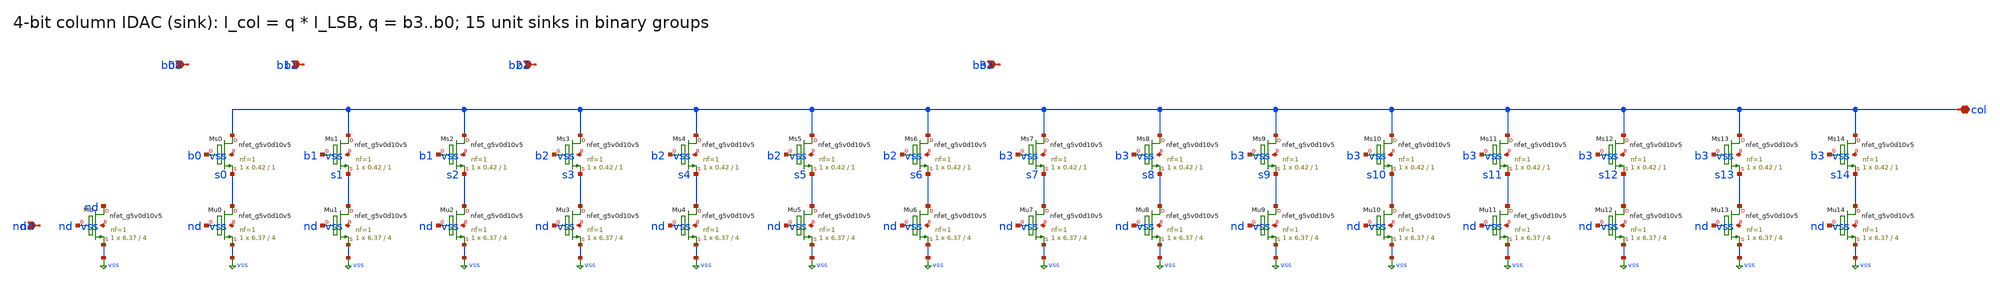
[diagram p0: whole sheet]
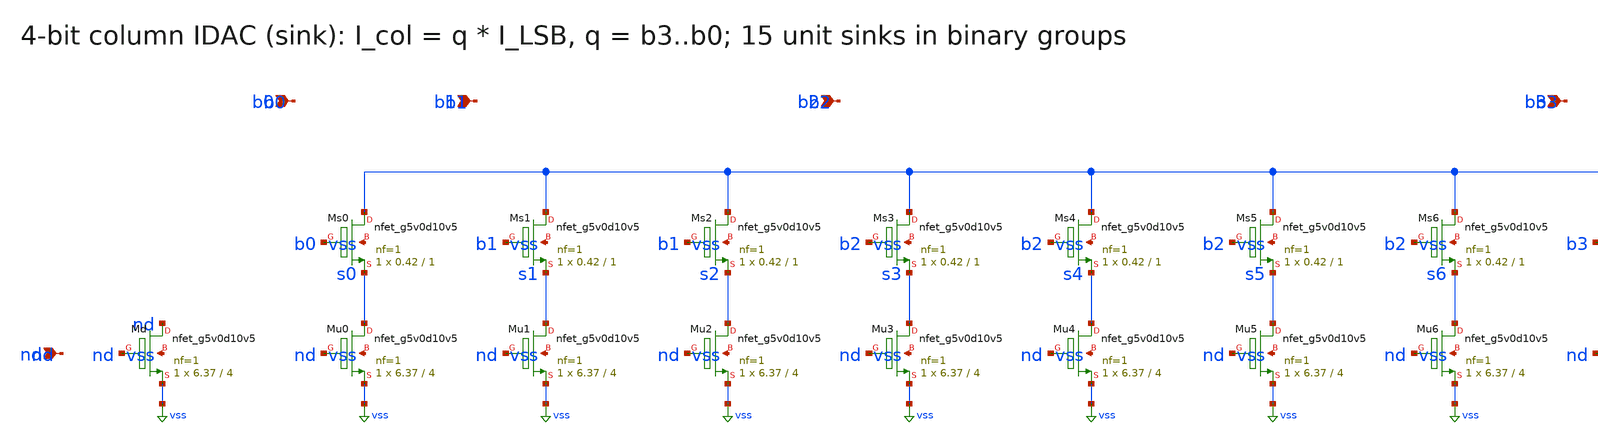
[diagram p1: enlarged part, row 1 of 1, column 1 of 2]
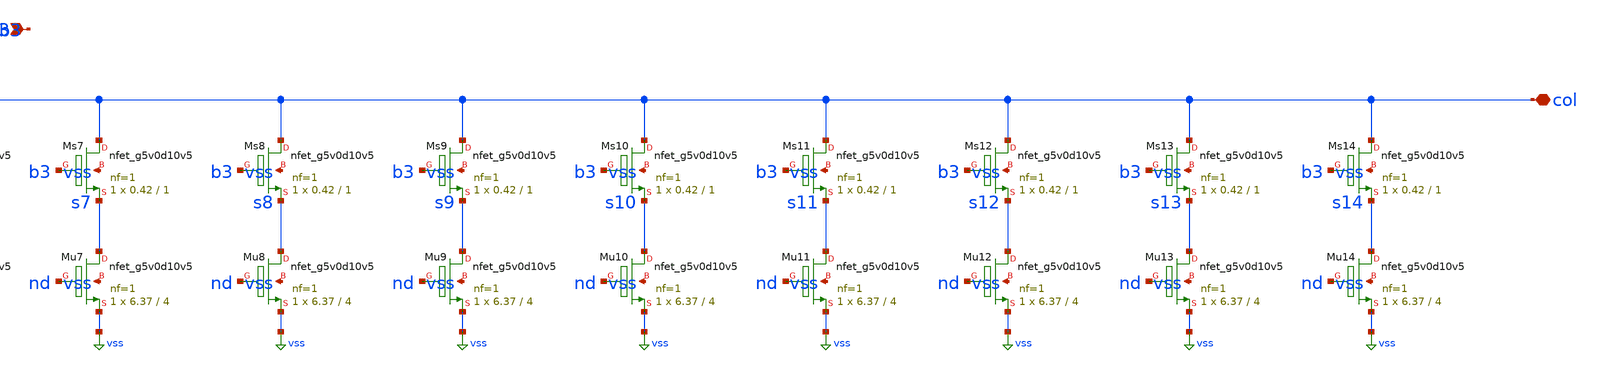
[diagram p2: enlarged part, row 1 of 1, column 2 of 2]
** sch_path: xschem/rt5w_idac4.sch
**.subckt rt5w_idac4 nd b0 b1 b2 b3 col
*.ipin nd
*.ipin b0
*.ipin b1
*.ipin b2
*.ipin b3
*.iopin col
XMd nd nd vss vss sky130_fd_pr__nfet_g5v0d10v5 L=4 W=6.37 nf=1 ad=1.847 as=1.847 pd=13.32 ps=13.32
+ nrd=0.04553 nrs=0.04553 sa=0 sb=0 sd=0 mult=1 m=1
XMu0 s0 nd vss vss sky130_fd_pr__nfet_g5v0d10v5 L=4 W=6.37 nf=1 ad=1.847 as=1.847 pd=13.32 ps=13.32
+ nrd=0.04553 nrs=0.04553 sa=0 sb=0 sd=0 mult=1 m=1
XMs0 col b0 s0 vss sky130_fd_pr__nfet_g5v0d10v5 L=1 W=0.42 nf=1 ad=0.1218 as=0.1218 pd=1.42 ps=1.42
+ nrd=0.6905 nrs=0.6905 sa=0 sb=0 sd=0 mult=1 m=1
XMu1 s1 nd vss vss sky130_fd_pr__nfet_g5v0d10v5 L=4 W=6.37 nf=1 ad=1.847 as=1.847 pd=13.32 ps=13.32
+ nrd=0.04553 nrs=0.04553 sa=0 sb=0 sd=0 mult=1 m=1
XMs1 col b1 s1 vss sky130_fd_pr__nfet_g5v0d10v5 L=1 W=0.42 nf=1 ad=0.1218 as=0.1218 pd=1.42 ps=1.42
+ nrd=0.6905 nrs=0.6905 sa=0 sb=0 sd=0 mult=1 m=1
XMu2 s2 nd vss vss sky130_fd_pr__nfet_g5v0d10v5 L=4 W=6.37 nf=1 ad=1.847 as=1.847 pd=13.32 ps=13.32
+ nrd=0.04553 nrs=0.04553 sa=0 sb=0 sd=0 mult=1 m=1
XMs2 col b1 s2 vss sky130_fd_pr__nfet_g5v0d10v5 L=1 W=0.42 nf=1 ad=0.1218 as=0.1218 pd=1.42 ps=1.42
+ nrd=0.6905 nrs=0.6905 sa=0 sb=0 sd=0 mult=1 m=1
XMu3 s3 nd vss vss sky130_fd_pr__nfet_g5v0d10v5 L=4 W=6.37 nf=1 ad=1.847 as=1.847 pd=13.32 ps=13.32
+ nrd=0.04553 nrs=0.04553 sa=0 sb=0 sd=0 mult=1 m=1
XMs3 col b2 s3 vss sky130_fd_pr__nfet_g5v0d10v5 L=1 W=0.42 nf=1 ad=0.1218 as=0.1218 pd=1.42 ps=1.42
+ nrd=0.6905 nrs=0.6905 sa=0 sb=0 sd=0 mult=1 m=1
XMu4 s4 nd vss vss sky130_fd_pr__nfet_g5v0d10v5 L=4 W=6.37 nf=1 ad=1.847 as=1.847 pd=13.32 ps=13.32
+ nrd=0.04553 nrs=0.04553 sa=0 sb=0 sd=0 mult=1 m=1
XMs4 col b2 s4 vss sky130_fd_pr__nfet_g5v0d10v5 L=1 W=0.42 nf=1 ad=0.1218 as=0.1218 pd=1.42 ps=1.42
+ nrd=0.6905 nrs=0.6905 sa=0 sb=0 sd=0 mult=1 m=1
XMu5 s5 nd vss vss sky130_fd_pr__nfet_g5v0d10v5 L=4 W=6.37 nf=1 ad=1.847 as=1.847 pd=13.32 ps=13.32
+ nrd=0.04553 nrs=0.04553 sa=0 sb=0 sd=0 mult=1 m=1
XMs5 col b2 s5 vss sky130_fd_pr__nfet_g5v0d10v5 L=1 W=0.42 nf=1 ad=0.1218 as=0.1218 pd=1.42 ps=1.42
+ nrd=0.6905 nrs=0.6905 sa=0 sb=0 sd=0 mult=1 m=1
XMu6 s6 nd vss vss sky130_fd_pr__nfet_g5v0d10v5 L=4 W=6.37 nf=1 ad=1.847 as=1.847 pd=13.32 ps=13.32
+ nrd=0.04553 nrs=0.04553 sa=0 sb=0 sd=0 mult=1 m=1
XMs6 col b2 s6 vss sky130_fd_pr__nfet_g5v0d10v5 L=1 W=0.42 nf=1 ad=0.1218 as=0.1218 pd=1.42 ps=1.42
+ nrd=0.6905 nrs=0.6905 sa=0 sb=0 sd=0 mult=1 m=1
XMu7 s7 nd vss vss sky130_fd_pr__nfet_g5v0d10v5 L=4 W=6.37 nf=1 ad=1.847 as=1.847 pd=13.32 ps=13.32
+ nrd=0.04553 nrs=0.04553 sa=0 sb=0 sd=0 mult=1 m=1
XMs7 col b3 s7 vss sky130_fd_pr__nfet_g5v0d10v5 L=1 W=0.42 nf=1 ad=0.1218 as=0.1218 pd=1.42 ps=1.42
+ nrd=0.6905 nrs=0.6905 sa=0 sb=0 sd=0 mult=1 m=1
XMu8 s8 nd vss vss sky130_fd_pr__nfet_g5v0d10v5 L=4 W=6.37 nf=1 ad=1.847 as=1.847 pd=13.32 ps=13.32
+ nrd=0.04553 nrs=0.04553 sa=0 sb=0 sd=0 mult=1 m=1
XMs8 col b3 s8 vss sky130_fd_pr__nfet_g5v0d10v5 L=1 W=0.42 nf=1 ad=0.1218 as=0.1218 pd=1.42 ps=1.42
+ nrd=0.6905 nrs=0.6905 sa=0 sb=0 sd=0 mult=1 m=1
XMu9 s9 nd vss vss sky130_fd_pr__nfet_g5v0d10v5 L=4 W=6.37 nf=1 ad=1.847 as=1.847 pd=13.32 ps=13.32
+ nrd=0.04553 nrs=0.04553 sa=0 sb=0 sd=0 mult=1 m=1
XMs9 col b3 s9 vss sky130_fd_pr__nfet_g5v0d10v5 L=1 W=0.42 nf=1 ad=0.1218 as=0.1218 pd=1.42 ps=1.42
+ nrd=0.6905 nrs=0.6905 sa=0 sb=0 sd=0 mult=1 m=1
XMu10 s10 nd vss vss sky130_fd_pr__nfet_g5v0d10v5 L=4 W=6.37 nf=1 ad=1.847 as=1.847 pd=13.32
+ ps=13.32 nrd=0.04553 nrs=0.04553 sa=0 sb=0 sd=0 mult=1 m=1
XMs10 col b3 s10 vss sky130_fd_pr__nfet_g5v0d10v5 L=1 W=0.42 nf=1 ad=0.1218 as=0.1218 pd=1.42
+ ps=1.42 nrd=0.6905 nrs=0.6905 sa=0 sb=0 sd=0 mult=1 m=1
XMu11 s11 nd vss vss sky130_fd_pr__nfet_g5v0d10v5 L=4 W=6.37 nf=1 ad=1.847 as=1.847 pd=13.32
+ ps=13.32 nrd=0.04553 nrs=0.04553 sa=0 sb=0 sd=0 mult=1 m=1
XMs11 col b3 s11 vss sky130_fd_pr__nfet_g5v0d10v5 L=1 W=0.42 nf=1 ad=0.1218 as=0.1218 pd=1.42
+ ps=1.42 nrd=0.6905 nrs=0.6905 sa=0 sb=0 sd=0 mult=1 m=1
XMu12 s12 nd vss vss sky130_fd_pr__nfet_g5v0d10v5 L=4 W=6.37 nf=1 ad=1.847 as=1.847 pd=13.32
+ ps=13.32 nrd=0.04553 nrs=0.04553 sa=0 sb=0 sd=0 mult=1 m=1
XMs12 col b3 s12 vss sky130_fd_pr__nfet_g5v0d10v5 L=1 W=0.42 nf=1 ad=0.1218 as=0.1218 pd=1.42
+ ps=1.42 nrd=0.6905 nrs=0.6905 sa=0 sb=0 sd=0 mult=1 m=1
XMu13 s13 nd vss vss sky130_fd_pr__nfet_g5v0d10v5 L=4 W=6.37 nf=1 ad=1.847 as=1.847 pd=13.32
+ ps=13.32 nrd=0.04553 nrs=0.04553 sa=0 sb=0 sd=0 mult=1 m=1
XMs13 col b3 s13 vss sky130_fd_pr__nfet_g5v0d10v5 L=1 W=0.42 nf=1 ad=0.1218 as=0.1218 pd=1.42
+ ps=1.42 nrd=0.6905 nrs=0.6905 sa=0 sb=0 sd=0 mult=1 m=1
XMu14 s14 nd vss vss sky130_fd_pr__nfet_g5v0d10v5 L=4 W=6.37 nf=1 ad=1.847 as=1.847 pd=13.32
+ ps=13.32 nrd=0.04553 nrs=0.04553 sa=0 sb=0 sd=0 mult=1 m=1
XMs14 col b3 s14 vss sky130_fd_pr__nfet_g5v0d10v5 L=1 W=0.42 nf=1 ad=0.1218 as=0.1218 pd=1.42
+ ps=1.42 nrd=0.6905 nrs=0.6905 sa=0 sb=0 sd=0 mult=1 m=1
**.ends
.GLOBAL vss
.end
